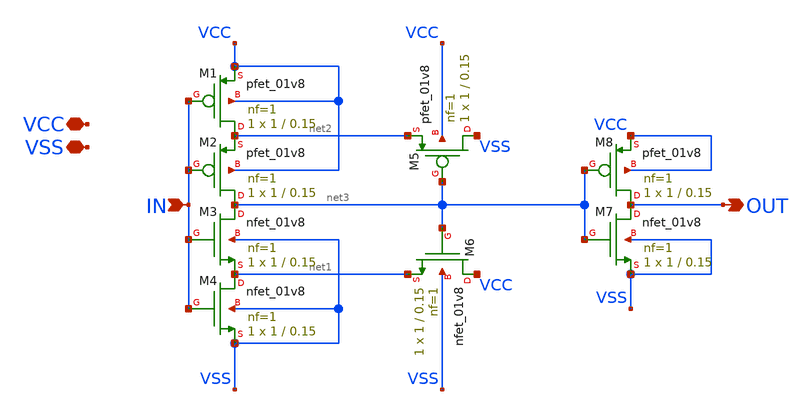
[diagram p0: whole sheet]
** sch_path: xschem/schmitt_trigger.sch
**.subckt schmitt_trigger IN OUT VCC VSS
*.ipin IN
*.opin OUT
*.iopin VCC
*.iopin VSS
XM1 net2 IN VCC VCC sky130_fd_pr__pfet_01v8 L=0.15 W=1 nf=1 ad='int((nf+1)/2) * W/nf * 0.29' as='int((nf+2)/2) * W/nf * 0.29'
+ pd='2*int((nf+1)/2) * (W/nf + 0.29)' ps='2*int((nf+2)/2) * (W/nf + 0.29)' nrd='0.29 / W' nrs='0.29 / W'
+ sa=0 sb=0 sd=0 mult=1 m=1
XM2 net3 IN net2 VCC sky130_fd_pr__pfet_01v8 L=0.15 W=1 nf=1 ad='int((nf+1)/2) * W/nf * 0.29' as='int((nf+2)/2) * W/nf * 0.29'
+ pd='2*int((nf+1)/2) * (W/nf + 0.29)' ps='2*int((nf+2)/2) * (W/nf + 0.29)' nrd='0.29 / W' nrs='0.29 / W'
+ sa=0 sb=0 sd=0 mult=1 m=1
XM3 net3 IN net1 VSS sky130_fd_pr__nfet_01v8 L=0.15 W=1 nf=1 ad='int((nf+1)/2) * W/nf * 0.29' as='int((nf+2)/2) * W/nf * 0.29'
+ pd='2*int((nf+1)/2) * (W/nf + 0.29)' ps='2*int((nf+2)/2) * (W/nf + 0.29)' nrd='0.29 / W' nrs='0.29 / W'
+ sa=0 sb=0 sd=0 mult=1 m=1
XM4 net1 IN VSS VSS sky130_fd_pr__nfet_01v8 L=0.15 W=1 nf=1 ad='int((nf+1)/2) * W/nf * 0.29' as='int((nf+2)/2) * W/nf * 0.29'
+ pd='2*int((nf+1)/2) * (W/nf + 0.29)' ps='2*int((nf+2)/2) * (W/nf + 0.29)' nrd='0.29 / W' nrs='0.29 / W'
+ sa=0 sb=0 sd=0 mult=1 m=1
XM5 VSS net3 net2 VCC sky130_fd_pr__pfet_01v8 L=0.15 W=1 nf=1 ad='int((nf+1)/2) * W/nf * 0.29' as='int((nf+2)/2) * W/nf * 0.29'
+ pd='2*int((nf+1)/2) * (W/nf + 0.29)' ps='2*int((nf+2)/2) * (W/nf + 0.29)' nrd='0.29 / W' nrs='0.29 / W'
+ sa=0 sb=0 sd=0 mult=1 m=1
XM6 VCC net3 net1 VSS sky130_fd_pr__nfet_01v8 L=0.15 W=1 nf=1 ad='int((nf+1)/2) * W/nf * 0.29' as='int((nf+2)/2) * W/nf * 0.29'
+ pd='2*int((nf+1)/2) * (W/nf + 0.29)' ps='2*int((nf+2)/2) * (W/nf + 0.29)' nrd='0.29 / W' nrs='0.29 / W'
+ sa=0 sb=0 sd=0 mult=1 m=1
XM7 OUT net3 VSS VSS sky130_fd_pr__nfet_01v8 L=0.15 W=1 nf=1 ad='int((nf+1)/2) * W/nf * 0.29' as='int((nf+2)/2) * W/nf * 0.29'
+ pd='2*int((nf+1)/2) * (W/nf + 0.29)' ps='2*int((nf+2)/2) * (W/nf + 0.29)' nrd='0.29 / W' nrs='0.29 / W'
+ sa=0 sb=0 sd=0 mult=1 m=1
XM8 OUT net3 VCC VCC sky130_fd_pr__pfet_01v8 L=0.15 W=1 nf=1 ad='int((nf+1)/2) * W/nf * 0.29' as='int((nf+2)/2) * W/nf * 0.29'
+ pd='2*int((nf+1)/2) * (W/nf + 0.29)' ps='2*int((nf+2)/2) * (W/nf + 0.29)' nrd='0.29 / W' nrs='0.29 / W'
+ sa=0 sb=0 sd=0 mult=1 m=1
**.ends
.end
